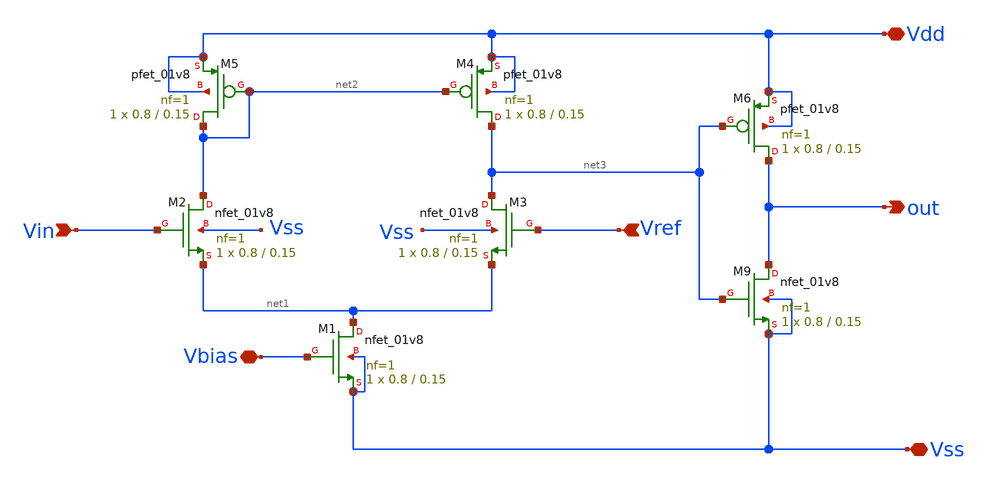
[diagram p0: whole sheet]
** sch_path: Week5/images/pre-layout_1bitADC/comparator.sch
**.subckt comparator Vdd Vss out Vin Vref Vbias
*.iopin Vdd
*.iopin Vss
*.opin out
*.ipin Vin
*.ipin Vref
*.iopin Vbias
XM1 net1 Vbias Vss Vss sky130_fd_pr__nfet_01v8 L=0.15 W=0.8 nf=1 ad='int((nf+1)/2) * W/nf * 0.29' as='int((nf+2)/2) * W/nf * 0.29'
+ pd='2*int((nf+1)/2) * (W/nf + 0.29)' ps='2*int((nf+2)/2) * (W/nf + 0.29)' nrd='0.29 / W' nrs='0.29 / W'
+ sa=0 sb=0 sd=0 mult=1 m=1
XM2 net2 Vin net1 Vss sky130_fd_pr__nfet_01v8 L=0.15 W=0.8 nf=1 ad='int((nf+1)/2) * W/nf * 0.29' as='int((nf+2)/2) * W/nf * 0.29'
+ pd='2*int((nf+1)/2) * (W/nf + 0.29)' ps='2*int((nf+2)/2) * (W/nf + 0.29)' nrd='0.29 / W' nrs='0.29 / W'
+ sa=0 sb=0 sd=0 mult=1 m=1
XM3 net3 Vref net1 Vss sky130_fd_pr__nfet_01v8 L=0.15 W=0.8 nf=1 ad='int((nf+1)/2) * W/nf * 0.29' as='int((nf+2)/2) * W/nf * 0.29'
+ pd='2*int((nf+1)/2) * (W/nf + 0.29)' ps='2*int((nf+2)/2) * (W/nf + 0.29)' nrd='0.29 / W' nrs='0.29 / W'
+ sa=0 sb=0 sd=0 mult=1 m=1
XM4 net3 net2 Vdd Vdd sky130_fd_pr__pfet_01v8 L=0.15 W=0.8 nf=1 ad='int((nf+1)/2) * W/nf * 0.29' as='int((nf+2)/2) * W/nf * 0.29'
+ pd='2*int((nf+1)/2) * (W/nf + 0.29)' ps='2*int((nf+2)/2) * (W/nf + 0.29)' nrd='0.29 / W' nrs='0.29 / W'
+ sa=0 sb=0 sd=0 mult=1 m=1
XM5 net2 net2 Vdd Vdd sky130_fd_pr__pfet_01v8 L=0.15 W=0.8 nf=1 ad='int((nf+1)/2) * W/nf * 0.29' as='int((nf+2)/2) * W/nf * 0.29'
+ pd='2*int((nf+1)/2) * (W/nf + 0.29)' ps='2*int((nf+2)/2) * (W/nf + 0.29)' nrd='0.29 / W' nrs='0.29 / W'
+ sa=0 sb=0 sd=0 mult=1 m=1
XM6 out net3 Vdd Vdd sky130_fd_pr__pfet_01v8 L=0.15 W=0.8 nf=1 ad='int((nf+1)/2) * W/nf * 0.29' as='int((nf+2)/2) * W/nf * 0.29'
+ pd='2*int((nf+1)/2) * (W/nf + 0.29)' ps='2*int((nf+2)/2) * (W/nf + 0.29)' nrd='0.29 / W' nrs='0.29 / W'
+ sa=0 sb=0 sd=0 mult=1 m=1
XM9 out net3 Vss Vss sky130_fd_pr__nfet_01v8 L=0.15 W=0.8 nf=1 ad='int((nf+1)/2) * W/nf * 0.29' as='int((nf+2)/2) * W/nf * 0.29'
+ pd='2*int((nf+1)/2) * (W/nf + 0.29)' ps='2*int((nf+2)/2) * (W/nf + 0.29)' nrd='0.29 / W' nrs='0.29 / W'
+ sa=0 sb=0 sd=0 mult=1 m=1
**.ends
.end
